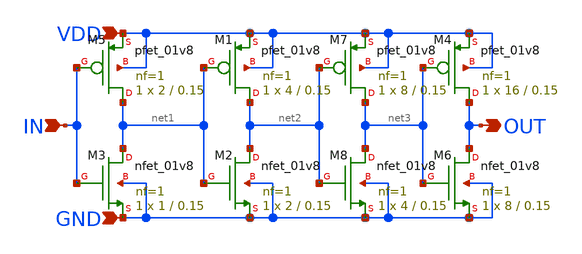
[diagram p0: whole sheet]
** sch_path: sch/BUFFER.sch
**.subckt BUFFER IN VDD GND OUT
*.ipin IN
*.ipin VDD
*.ipin GND
*.opin OUT
XM5 net1 IN VDD VDD sky130_fd_pr__pfet_01v8 L=0.15 W=2 nf=1 ad='int((1 + 1)/2) * 2 / 1 * 0.29' as='int((1 + 2)/2) * 2 / 1 * 0.29'
+ pd='2*int((1 + 1)/2) * (2 / 1 + 0.29)' ps='2*int((1 + 2)/2) * (2 / 1 + 0.29)' nrd='0.29 / 2 ' nrs='0.29 / 2 '
+ sa=0 sb=0 sd=0 mult=1 m=1
XM1 net2 net1 VDD VDD sky130_fd_pr__pfet_01v8 L=0.15 W=4 nf=1 ad='int((1 + 1)/2) * 4 / 1 * 0.29' as='int((1 + 2)/2) * 4 / 1 * 0.29'
+ pd='2*int((1 + 1)/2) * (4 / 1 + 0.29)' ps='2*int((1 + 2)/2) * (4 / 1 + 0.29)' nrd='0.29 / 4 ' nrs='0.29 / 4 '
+ sa=0 sb=0 sd=0 mult=1 m=1
XM2 net2 net1 GND GND sky130_fd_pr__nfet_01v8 L=0.15 W=2 nf=1 ad='int((1 + 1)/2) * 2 / 1 * 0.29' as='int((1 + 2)/2) * 2 / 1 * 0.29'
+ pd='2*int((1 + 1)/2) * (2 / 1 + 0.29)' ps='2*int((1 + 2)/2) * (2 / 1 + 0.29)' nrd='0.29 / 2 ' nrs='0.29 / 2 '
+ sa=0 sb=0 sd=0 mult=1 m=1
XM3 net1 IN GND GND sky130_fd_pr__nfet_01v8 L=0.15 W=1 nf=1 ad='int((1 + 1)/2) * 1 / 1 * 0.29' as='int((1 + 2)/2) * 1 / 1 * 0.29'
+ pd='2*int((1 + 1)/2) * (1 / 1 + 0.29)' ps='2*int((1 + 2)/2) * (1 / 1 + 0.29)' nrd='0.29 / 1 ' nrs='0.29 / 1 '
+ sa=0 sb=0 sd=0 mult=1 m=1
XM4 OUT net3 VDD VDD sky130_fd_pr__pfet_01v8 L=0.15 W=16 nf=1 ad='int((1 + 1)/2) * 16 / 1 * 0.29' as='int((1 + 2)/2) * 16 / 1 * 0.29'
+ pd='2*int((1 + 1)/2) * (16 / 1 + 0.29)' ps='2*int((1 + 2)/2) * (16 / 1 + 0.29)' nrd='0.29 / 16 ' nrs='0.29 / 16 '
+ sa=0 sb=0 sd=0 mult=1 m=1
XM6 OUT net3 GND GND sky130_fd_pr__nfet_01v8 L=0.15 W=8 nf=1 ad='int((1 + 1)/2) * 8 / 1 * 0.29' as='int((1 + 2)/2) * 8 / 1 * 0.29'
+ pd='2*int((1 + 1)/2) * (8 / 1 + 0.29)' ps='2*int((1 + 2)/2) * (8 / 1 + 0.29)' nrd='0.29 / 8 ' nrs='0.29 / 8 '
+ sa=0 sb=0 sd=0 mult=1 m=1
XM7 net3 net2 VDD VDD sky130_fd_pr__pfet_01v8 L=0.15 W=8 nf=1 ad='int((1 + 1)/2) * 8 / 1 * 0.29' as='int((1 + 2)/2) * 8 / 1 * 0.29'
+ pd='2*int((1 + 1)/2) * (8 / 1 + 0.29)' ps='2*int((1 + 2)/2) * (8 / 1 + 0.29)' nrd='0.29 / 8 ' nrs='0.29 / 8 '
+ sa=0 sb=0 sd=0 mult=1 m=1
XM8 net3 net2 GND GND sky130_fd_pr__nfet_01v8 L=0.15 W=4 nf=1 ad='int((1 + 1)/2) * 4 / 1 * 0.29' as='int((1 + 2)/2) * 4 / 1 * 0.29'
+ pd='2*int((1 + 1)/2) * (4 / 1 + 0.29)' ps='2*int((1 + 2)/2) * (4 / 1 + 0.29)' nrd='0.29 / 4 ' nrs='0.29 / 4 '
+ sa=0 sb=0 sd=0 mult=1 m=1
**.ends
.end
